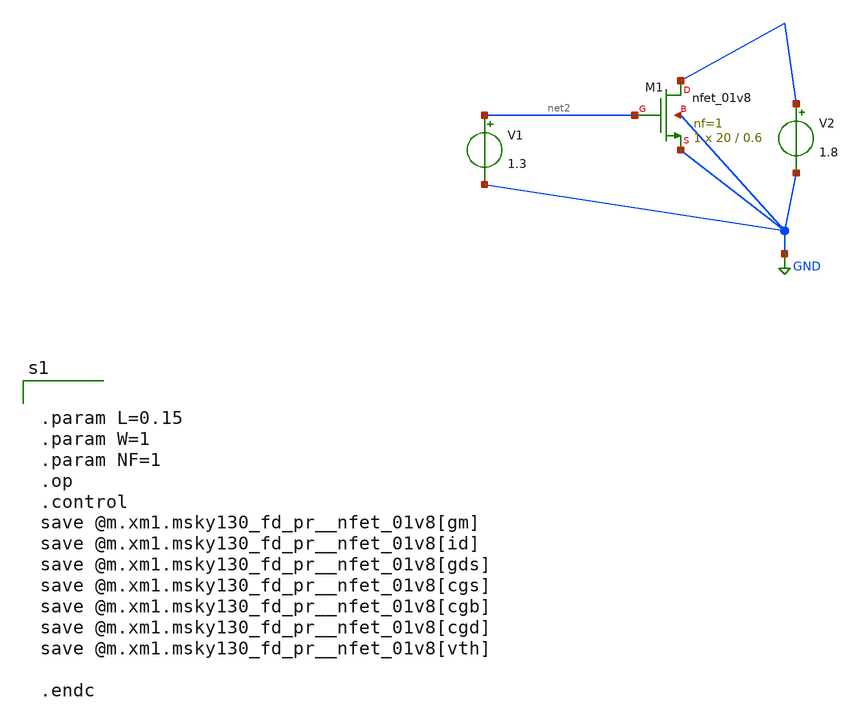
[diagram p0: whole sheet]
** sch_path: xschem/untitled-1.sch
**.subckt untitled-1
XM1 net1 net2 GND GND sky130_fd_pr__nfet_01v8 L=0.6 W=20 nf=1 ad='int((nf+1)/2) * W/nf * 0.29' as='int((nf+2)/2) * W/nf * 0.29'
+ pd='2*int((nf+1)/2) * (W/nf + 0.29)' ps='2*int((nf+2)/2) * (W/nf + 0.29)' nrd='0.29 / W' nrs='0.29 / W'
+ sa=0 sb=0 sd=0 mult=1 m=1
V1 net2 GND 1.3
V2 net1 GND 1.8
**** begin user architecture code
.lib $::SKYWATER_MODELS/sky130.lib.spice tt
.include $::PDKPATH/libs.ref/sky130_fd_sc_hvl/spice/sky130_fd_sc_hvl.spice


.param L=0.15
.param W=1
.param NF=1
.op
.control
save @m.xm1.msky130_fd_pr__nfet_01v8[gm]
save @m.xm1.msky130_fd_pr__nfet_01v8[id]
save @m.xm1.msky130_fd_pr__nfet_01v8[gds]
save @m.xm1.msky130_fd_pr__nfet_01v8[cgs]
save @m.xm1.msky130_fd_pr__nfet_01v8[cgb]
save @m.xm1.msky130_fd_pr__nfet_01v8[cgd]
save @m.xm1.msky130_fd_pr__nfet_01v8[vth]

.endc


**** end user architecture code
**.ends
.GLOBAL GND
.end
